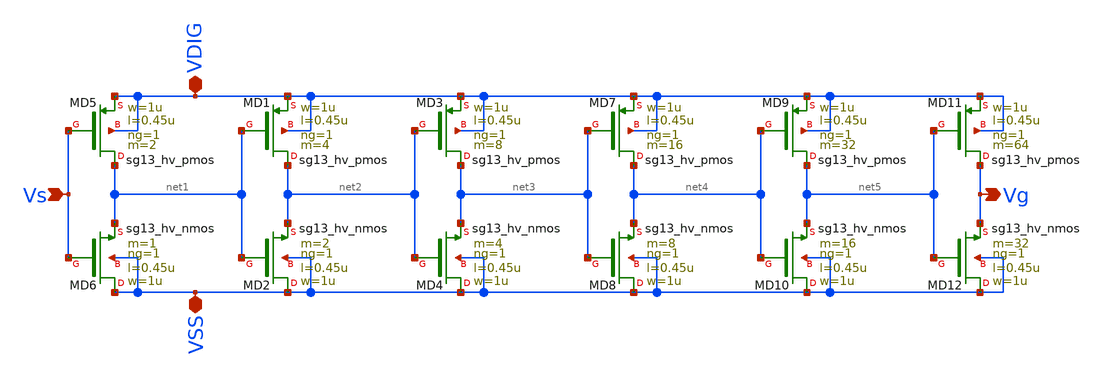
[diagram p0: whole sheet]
** sch_path: ChipUSM_AnalogTrack24/BUFFHV/BUFFHV_vto1p1.sch
**.subckt BUFFHV_vto1p1 VDIG Vs Vg VSS
*.iopin VDIG
*.ipin Vs
*.opin Vg
*.iopin VSS
XMD5 net1 Vs VDIG VDIG sg13_hv_pmos w=1u l=0.45u ng=1 m=2 mm_ok=1
XMD6 VSS Vs net1 VSS sg13_hv_nmos w=1u l=0.45u ng=1 m=1 mm_ok=1
XMD1 net2 net1 VDIG VDIG sg13_hv_pmos w=1u l=0.45u ng=1 m=4 mm_ok=1
XMD2 VSS net1 net2 VSS sg13_hv_nmos w=1u l=0.45u ng=1 m=2 mm_ok=1
XMD3 net3 net2 VDIG VDIG sg13_hv_pmos w=1u l=0.45u ng=1 m=8 mm_ok=1
XMD4 VSS net2 net3 VSS sg13_hv_nmos w=1u l=0.45u ng=1 m=4 mm_ok=1
XMD7 net4 net3 VDIG VDIG sg13_hv_pmos w=1u l=0.45u ng=1 m=16 mm_ok=1
XMD8 VSS net3 net4 VSS sg13_hv_nmos w=1u l=0.45u ng=1 m=8 mm_ok=1
XMD9 net5 net4 VDIG VDIG sg13_hv_pmos w=1u l=0.45u ng=1 m=32 mm_ok=1
XMD10 VSS net4 net5 VSS sg13_hv_nmos w=1u l=0.45u ng=1 m=16 mm_ok=1
XMD11 Vg net5 VDIG VDIG sg13_hv_pmos w=1u l=0.45u ng=1 m=64 mm_ok=1
XMD12 VSS net5 Vg VSS sg13_hv_nmos w=1u l=0.45u ng=1 m=32 mm_ok=1
**.ends
.end
